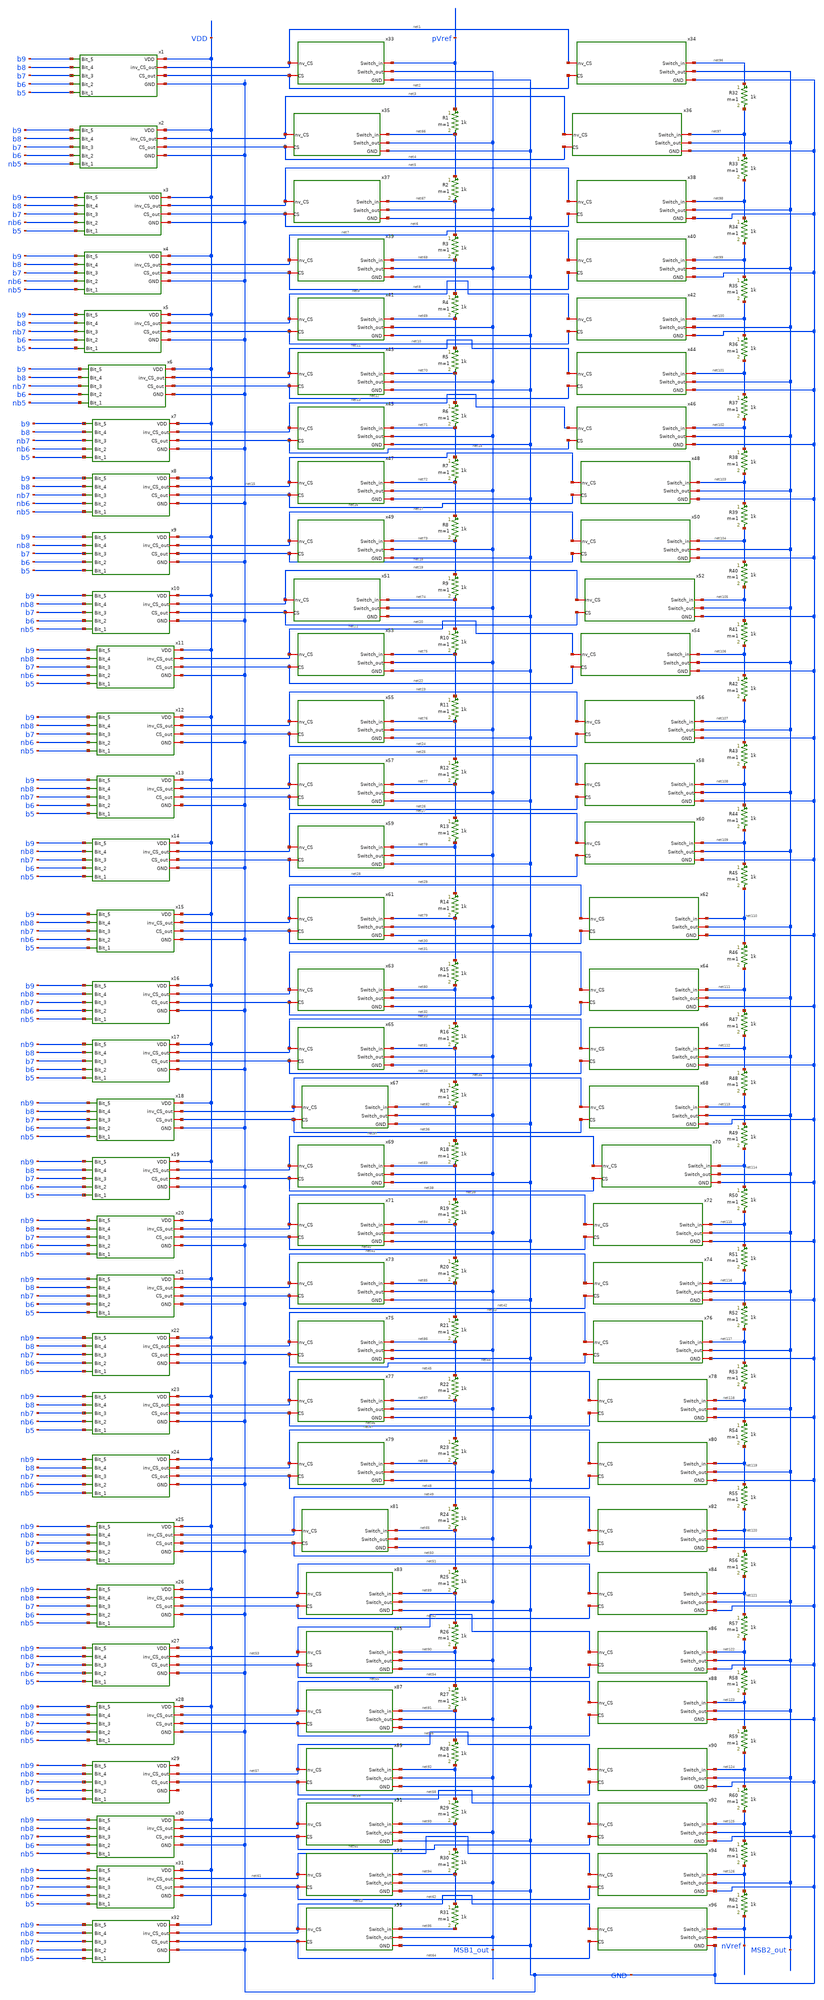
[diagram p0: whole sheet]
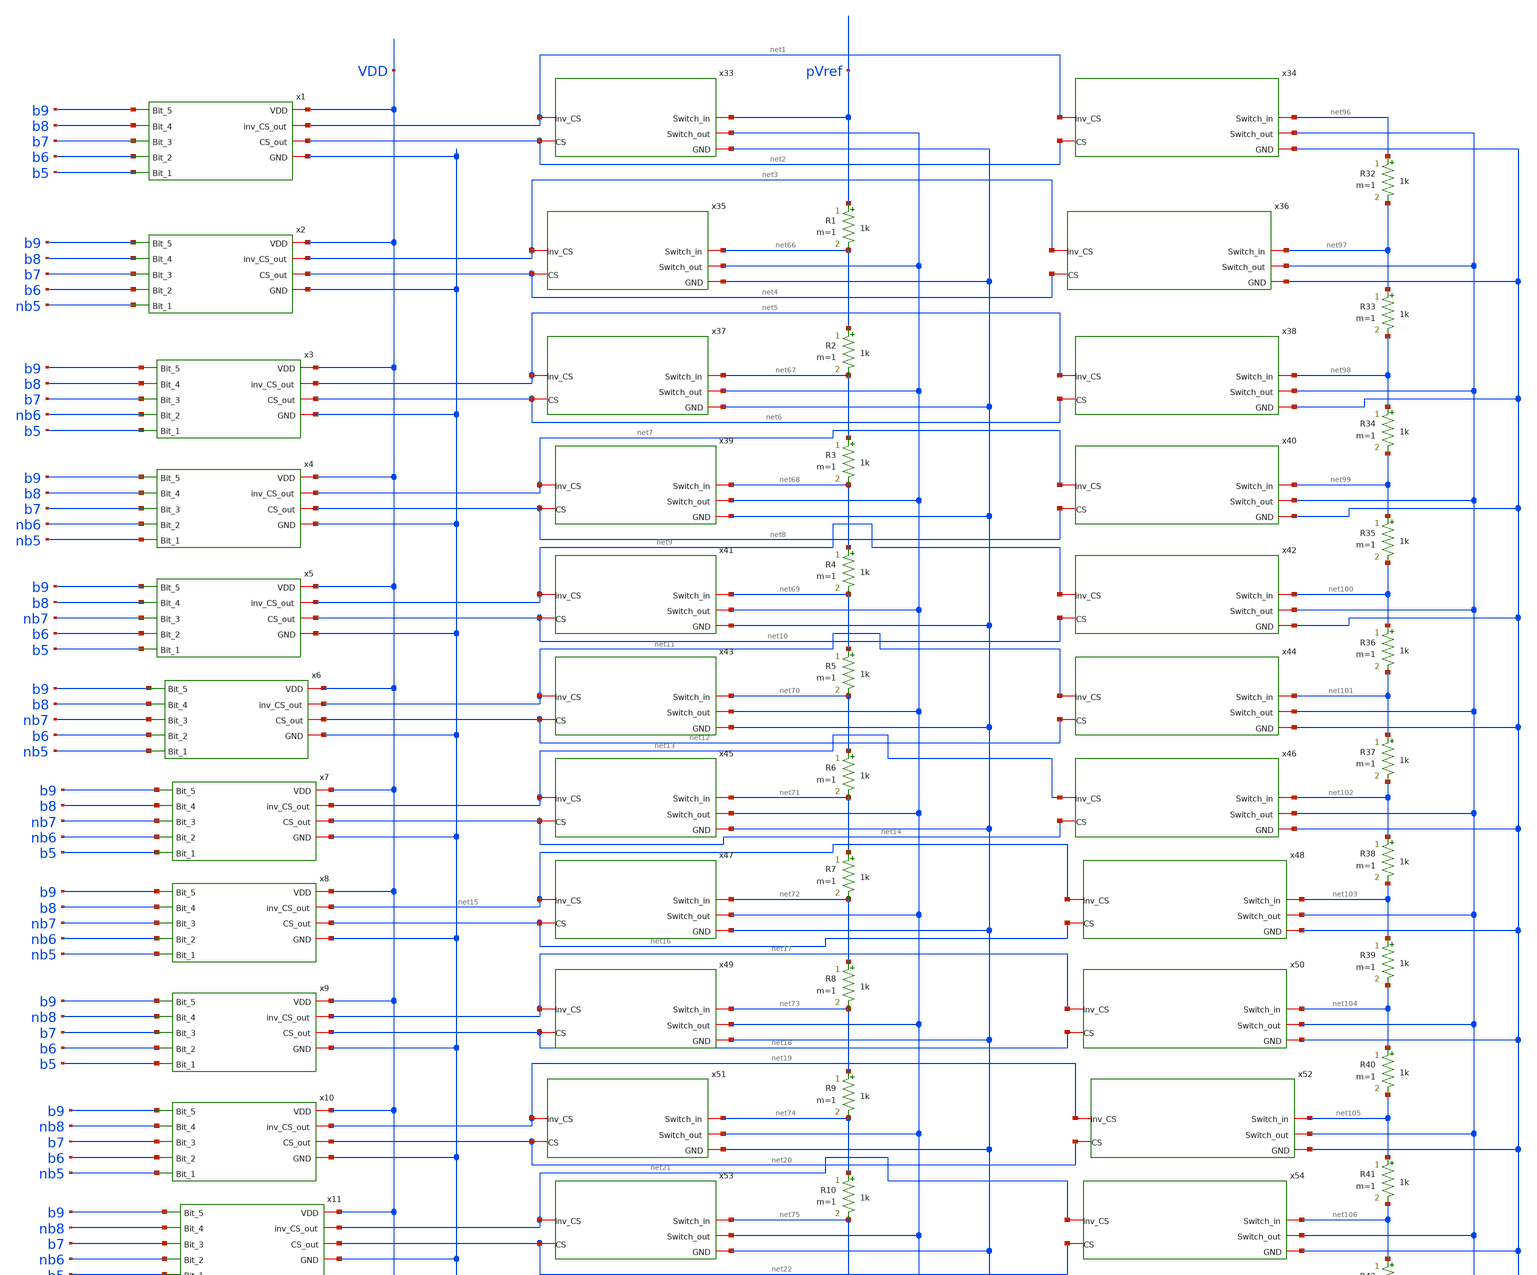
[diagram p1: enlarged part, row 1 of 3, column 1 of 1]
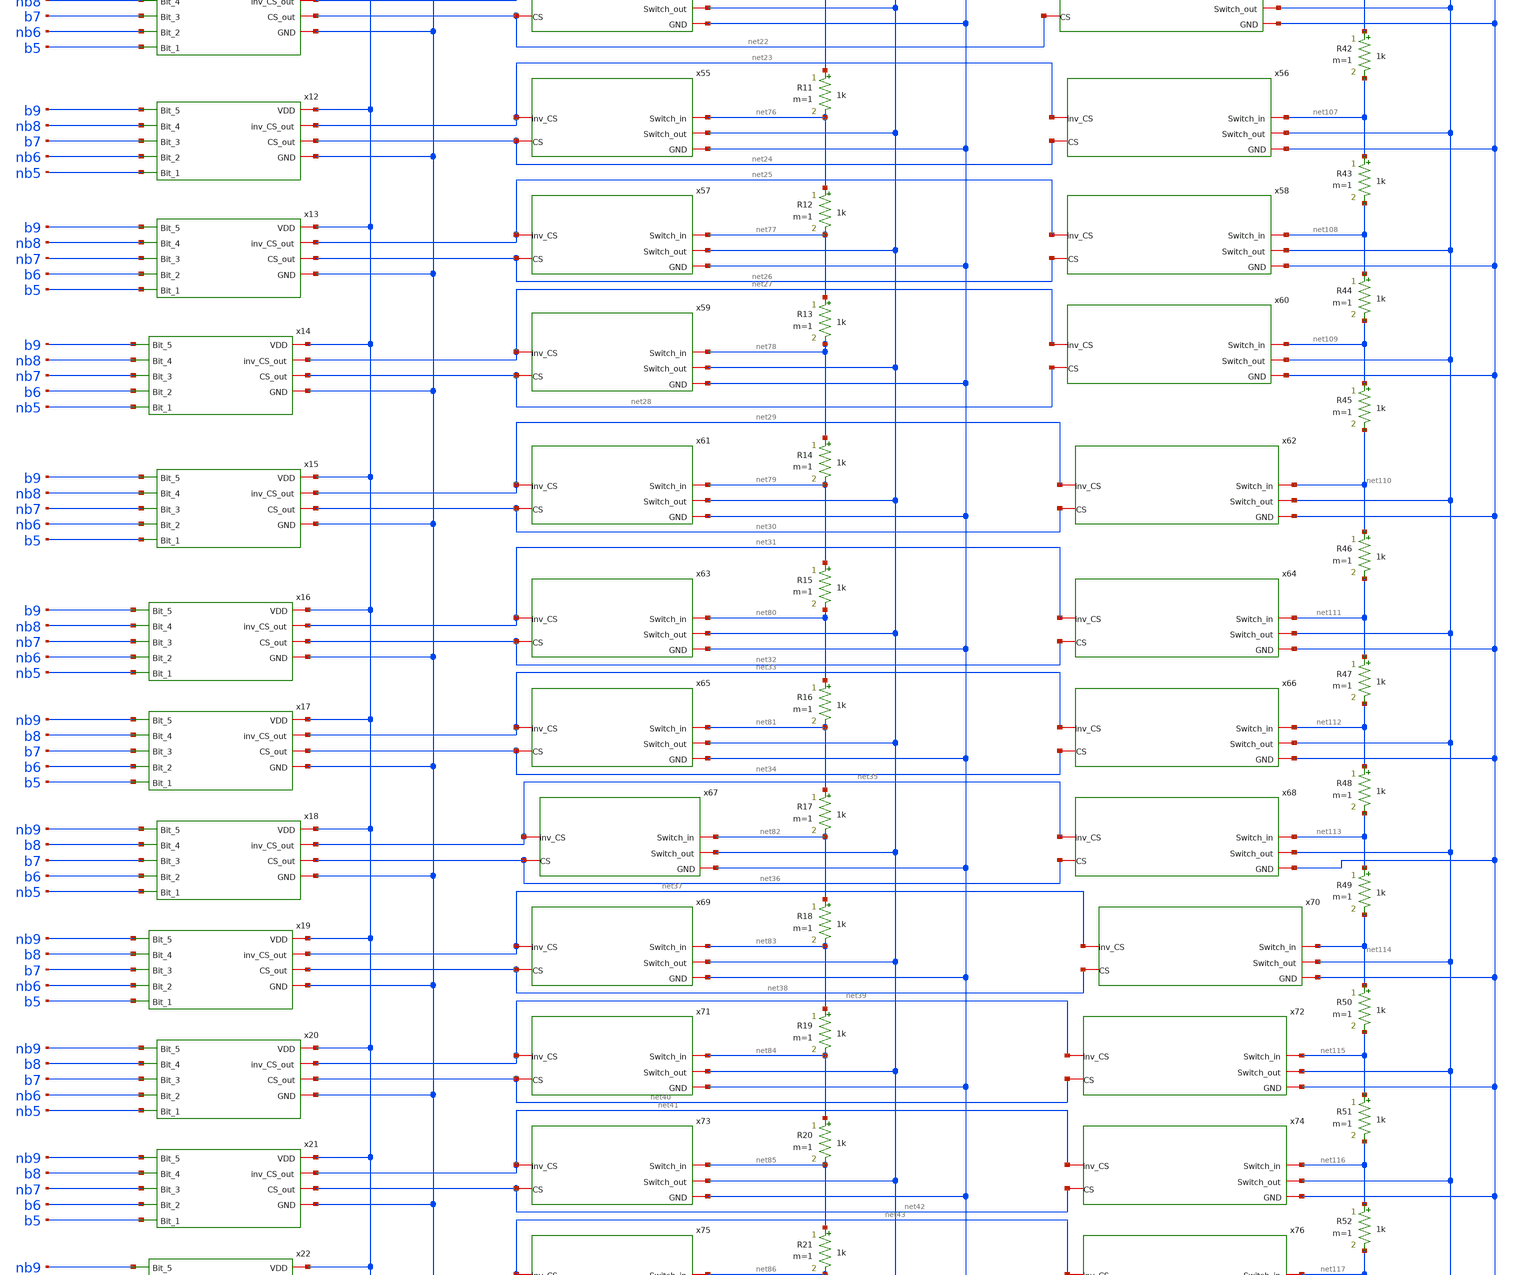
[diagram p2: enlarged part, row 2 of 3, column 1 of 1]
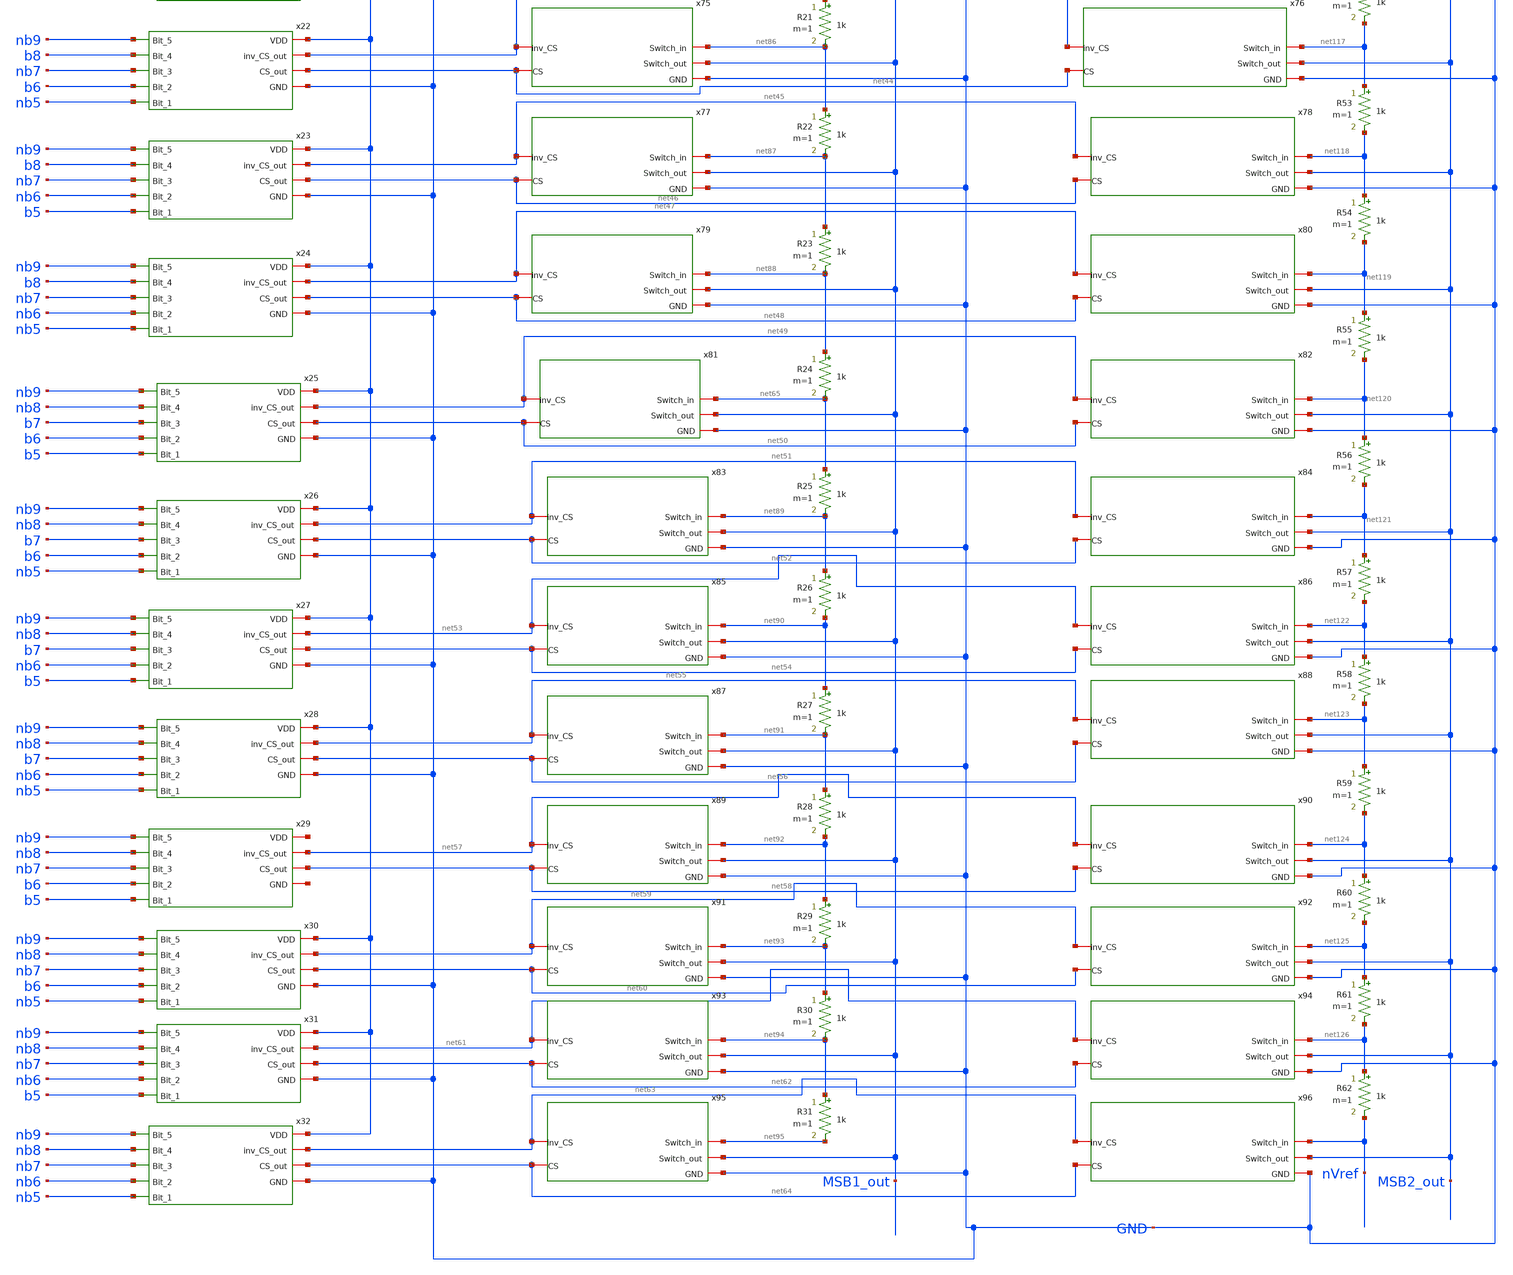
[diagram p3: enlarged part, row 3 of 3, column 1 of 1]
** sch_path: ProjectDesigns/10bitDAC/MSB.sch
**.subckt MSB
x1 VDD net1 b9 b8 net2 b7 b6 b5 GND 5bit_AND
x3 VDD net5 b9 b8 net6 b7 nb6 b5 GND 5bit_AND
x4 VDD net7 b9 b8 net8 b7 nb6 nb5 GND 5bit_AND
x5 VDD net9 b9 b8 net10 nb7 b6 b5 GND 5bit_AND
x6 VDD net11 b9 b8 net12 nb7 b6 nb5 GND 5bit_AND
x7 VDD net13 b9 b8 net14 nb7 nb6 b5 GND 5bit_AND
x8 VDD net15 b9 b8 net16 nb7 nb6 nb5 GND 5bit_AND
x9 VDD net17 b9 nb8 net18 b7 b6 b5 GND 5bit_AND
x2 VDD net3 b9 b8 net4 b7 b6 nb5 GND 5bit_AND
x10 VDD net19 b9 nb8 net20 b7 b6 nb5 GND 5bit_AND
x11 VDD net21 b9 nb8 net22 b7 nb6 b5 GND 5bit_AND
x12 VDD net23 b9 nb8 net24 b7 nb6 nb5 GND 5bit_AND
x13 VDD net25 b9 nb8 net26 nb7 b6 b5 GND 5bit_AND
x14 VDD net27 b9 nb8 net28 nb7 b6 nb5 GND 5bit_AND
x15 VDD net29 b9 nb8 net30 nb7 nb6 b5 GND 5bit_AND
x16 VDD net31 b9 nb8 net32 nb7 nb6 nb5 GND 5bit_AND
x17 VDD net33 nb9 b8 net34 b7 b6 b5 GND 5bit_AND
x18 VDD net35 nb9 b8 net36 b7 b6 nb5 GND 5bit_AND
x19 VDD net37 nb9 b8 net38 b7 nb6 b5 GND 5bit_AND
x20 VDD net39 nb9 b8 net40 b7 nb6 nb5 GND 5bit_AND
x21 VDD net41 nb9 b8 net42 nb7 b6 b5 GND 5bit_AND
x22 VDD net43 nb9 b8 net44 nb7 b6 nb5 GND 5bit_AND
x23 VDD net45 nb9 b8 net46 nb7 nb6 b5 GND 5bit_AND
x24 VDD net47 nb9 b8 net48 nb7 nb6 nb5 GND 5bit_AND
x25 VDD net49 nb9 nb8 net50 b7 b6 b5 GND 5bit_AND
x26 VDD net51 nb9 nb8 net52 b7 b6 nb5 GND 5bit_AND
x27 VDD net53 nb9 nb8 net54 b7 nb6 b5 GND 5bit_AND
x28 VDD net55 nb9 nb8 net56 b7 nb6 nb5 GND 5bit_AND
x29 net127 net57 nb9 nb8 net58 nb7 b6 b5 net128 5bit_AND
x30 VDD net59 nb9 nb8 net60 nb7 b6 nb5 GND 5bit_AND
x31 VDD net61 nb9 nb8 net62 nb7 nb6 b5 GND 5bit_AND
x32 VDD net63 nb9 nb8 net64 nb7 nb6 nb5 GND 5bit_AND
x33 net1 net2 pVref MSB1_out GND Switch
x34 net1 net2 net96 MSB2_out GND Switch
x35 net3 net4 net66 MSB1_out GND Switch
x36 net3 net4 net97 MSB2_out GND Switch
x37 net5 net6 net67 MSB1_out GND Switch
x38 net5 net6 net98 MSB2_out GND Switch
x39 net7 net8 net68 MSB1_out GND Switch
x40 net7 net8 net99 MSB2_out GND Switch
x41 net9 net10 net69 MSB1_out GND Switch
x42 net9 net10 net100 MSB2_out GND Switch
x43 net11 net12 net70 MSB1_out GND Switch
x44 net11 net12 net101 MSB2_out GND Switch
x45 net13 net14 net71 MSB1_out GND Switch
x46 net13 net14 net102 MSB2_out GND Switch
x47 net15 net16 net72 MSB1_out GND Switch
x48 net15 net16 net103 MSB2_out GND Switch
x49 net17 net18 net73 MSB1_out GND Switch
x50 net17 net18 net104 MSB2_out GND Switch
x51 net19 net20 net74 MSB1_out GND Switch
x52 net19 net20 net105 MSB2_out GND Switch
x53 net21 net22 net75 MSB1_out GND Switch
x54 net21 net22 net106 MSB2_out GND Switch
x55 net23 net24 net76 MSB1_out GND Switch
x56 net23 net24 net107 MSB2_out GND Switch
x57 net25 net26 net77 MSB1_out GND Switch
x58 net25 net26 net108 MSB2_out GND Switch
x59 net27 net28 net78 MSB1_out GND Switch
x60 net27 net28 net109 MSB2_out GND Switch
x61 net29 net30 net79 MSB1_out GND Switch
x62 net29 net30 net110 MSB2_out GND Switch
x63 net31 net32 net80 MSB1_out GND Switch
x64 net31 net32 net111 MSB2_out GND Switch
x65 net33 net34 net81 MSB1_out GND Switch
x66 net33 net34 net112 MSB2_out GND Switch
x67 net35 net36 net82 MSB1_out GND Switch
x68 net35 net36 net113 MSB2_out GND Switch
x69 net37 net38 net83 MSB1_out GND Switch
x70 net37 net38 net114 MSB2_out GND Switch
x71 net39 net40 net84 MSB1_out GND Switch
x72 net39 net40 net115 MSB2_out GND Switch
x73 net41 net42 net85 MSB1_out GND Switch
x74 net41 net42 net116 MSB2_out GND Switch
x75 net43 net44 net86 MSB1_out GND Switch
x76 net43 net44 net117 MSB2_out GND Switch
x77 net45 net46 net87 MSB1_out GND Switch
x78 net45 net46 net118 MSB2_out GND Switch
x79 net47 net48 net88 MSB1_out GND Switch
x80 net47 net48 net119 MSB2_out GND Switch
x81 net49 net50 net65 MSB1_out GND Switch
x82 net49 net50 net120 MSB2_out GND Switch
x83 net51 net52 net89 MSB1_out GND Switch
x84 net51 net52 net121 MSB2_out GND Switch
x85 net53 net54 net90 MSB1_out GND Switch
x86 net53 net54 net122 MSB2_out GND Switch
x87 net55 net56 net91 MSB1_out GND Switch
x88 net55 net56 net123 MSB2_out GND Switch
x89 net57 net58 net92 MSB1_out GND Switch
x90 net57 net58 net124 MSB2_out GND Switch
x91 net59 net60 net93 MSB1_out GND Switch
x92 net59 net60 net125 MSB2_out GND Switch
x93 net61 net62 net94 MSB1_out GND Switch
x94 net61 net62 net126 MSB2_out GND Switch
x95 net63 net64 net95 MSB1_out GND Switch
x96 net63 net64 nVref MSB2_out GND Switch
R1 pVref net66 1k m=1
R2 net66 net67 1k m=1
R3 net67 net68 1k m=1
R4 net68 net69 1k m=1
R5 net69 net70 1k m=1
R6 net70 net71 1k m=1
R7 net71 net72 1k m=1
R8 net72 net73 1k m=1
R9 net73 net74 1k m=1
R10 net74 net75 1k m=1
R11 net75 net76 1k m=1
R12 net76 net77 1k m=1
R13 net77 net78 1k m=1
R14 net78 net79 1k m=1
R15 net79 net80 1k m=1
R16 net80 net81 1k m=1
R17 net81 net82 1k m=1
R18 net82 net83 1k m=1
R19 net83 net84 1k m=1
R20 net84 net85 1k m=1
R21 net85 net86 1k m=1
R22 net86 net87 1k m=1
R23 net87 net88 1k m=1
R24 net88 net65 1k m=1
R25 net65 net89 1k m=1
R26 net89 net90 1k m=1
R27 net90 net91 1k m=1
R28 net91 net92 1k m=1
R29 net92 net93 1k m=1
R30 net93 net94 1k m=1
R31 net94 net95 1k m=1
R32 net96 net97 1k m=1
R33 net97 net98 1k m=1
R34 net98 net99 1k m=1
R35 net99 net100 1k m=1
R36 net100 net101 1k m=1
R37 net101 net102 1k m=1
R38 net102 net103 1k m=1
R39 net103 net104 1k m=1
R40 net104 net105 1k m=1
R41 net105 net106 1k m=1
R42 net106 net107 1k m=1
R43 net107 net108 1k m=1
R44 net108 net109 1k m=1
R45 net109 net110 1k m=1
R46 net110 net111 1k m=1
R47 net111 net112 1k m=1
R48 net112 net113 1k m=1
R49 net113 net114 1k m=1
R50 net114 net115 1k m=1
R51 net115 net116 1k m=1
R52 net116 net117 1k m=1
R53 net117 net118 1k m=1
R54 net118 net119 1k m=1
R55 net119 net120 1k m=1
R56 net120 net121 1k m=1
R57 net121 net122 1k m=1
R58 net122 net123 1k m=1
R59 net123 net124 1k m=1
R60 net124 net125 1k m=1
R61 net125 net126 1k m=1
R62 net126 nVref 1k m=1
**.ends

* expanding   symbol:  /home/shalini1234/Project/5bit_AND.sym # of pins=9
** sym_path: ProjectDesigns/5BitAND/5bit_AND.sym
** sch_path: ProjectDesigns/5BitAND/5bit_AND.sch
.subckt 5bit_AND VDD inv_CS_out Bit_5 Bit_4 CS_out Bit_3 Bit_2 Bit_1 GND
*.ipin Bit_1
*.ipin Bit_3
*.ipin Bit_2
*.ipin Bit_4
*.ipin Bit_5
*.iopin inv_CS_out
*.iopin CS_out
*.iopin VDD
*.iopin GND
XM1 inv_CS_out Bit_5 net1 net1 sky130_fd_pr__nfet_01v8 L=0.15 W=1 nf=1 ad='int((nf+1)/2) * W/nf * 0.29'
+ as='int((nf+2)/2) * W/nf * 0.29' pd='2*int((nf+1)/2) * (W/nf + 0.29)' ps='2*int((nf+2)/2) * (W/nf + 0.29)'
+ nrd='0.29 / W' nrs='0.29 / W' sa=0 sb=0 sd=0 mult=1 m=1
XM2 net1 Bit_4 net2 net2 sky130_fd_pr__nfet_01v8 L=0.15 W=1 nf=1 ad='int((nf+1)/2) * W/nf * 0.29' as='int((nf+2)/2) * W/nf * 0.29'
+ pd='2*int((nf+1)/2) * (W/nf + 0.29)' ps='2*int((nf+2)/2) * (W/nf + 0.29)' nrd='0.29 / W' nrs='0.29 / W'
+ sa=0 sb=0 sd=0 mult=1 m=1
XM3 net2 Bit_3 net3 net3 sky130_fd_pr__nfet_01v8 L=0.15 W=1 nf=1 ad='int((nf+1)/2) * W/nf * 0.29' as='int((nf+2)/2) * W/nf * 0.29'
+ pd='2*int((nf+1)/2) * (W/nf + 0.29)' ps='2*int((nf+2)/2) * (W/nf + 0.29)' nrd='0.29 / W' nrs='0.29 / W'
+ sa=0 sb=0 sd=0 mult=1 m=1
XM4 net3 Bit_2 net4 net4 sky130_fd_pr__nfet_01v8 L=0.15 W=1 nf=1 ad='int((nf+1)/2) * W/nf * 0.29' as='int((nf+2)/2) * W/nf * 0.29'
+ pd='2*int((nf+1)/2) * (W/nf + 0.29)' ps='2*int((nf+2)/2) * (W/nf + 0.29)' nrd='0.29 / W' nrs='0.29 / W'
+ sa=0 sb=0 sd=0 mult=1 m=1
XM5 net4 Bit_1 GND GND sky130_fd_pr__nfet_01v8 L=0.15 W=1 nf=1 ad='int((nf+1)/2) * W/nf * 0.29' as='int((nf+2)/2) * W/nf * 0.29'
+ pd='2*int((nf+1)/2) * (W/nf + 0.29)' ps='2*int((nf+2)/2) * (W/nf + 0.29)' nrd='0.29 / W' nrs='0.29 / W'
+ sa=0 sb=0 sd=0 mult=1 m=1
XM6 inv_CS_out Bit_3 VDD VDD sky130_fd_pr__pfet_01v8 L=0.15 W=1 nf=1 ad='int((nf+1)/2) * W/nf * 0.29'
+ as='int((nf+2)/2) * W/nf * 0.29' pd='2*int((nf+1)/2) * (W/nf + 0.29)' ps='2*int((nf+2)/2) * (W/nf + 0.29)'
+ nrd='0.29 / W' nrs='0.29 / W' sa=0 sb=0 sd=0 mult=1 m=1
XM7 inv_CS_out Bit_2 VDD VDD sky130_fd_pr__pfet_01v8 L=0.15 W=1 nf=1 ad='int((nf+1)/2) * W/nf * 0.29'
+ as='int((nf+2)/2) * W/nf * 0.29' pd='2*int((nf+1)/2) * (W/nf + 0.29)' ps='2*int((nf+2)/2) * (W/nf + 0.29)'
+ nrd='0.29 / W' nrs='0.29 / W' sa=0 sb=0 sd=0 mult=1 m=1
XM8 inv_CS_out Bit_1 VDD VDD sky130_fd_pr__pfet_01v8 L=0.15 W=1 nf=1 ad='int((nf+1)/2) * W/nf * 0.29'
+ as='int((nf+2)/2) * W/nf * 0.29' pd='2*int((nf+1)/2) * (W/nf + 0.29)' ps='2*int((nf+2)/2) * (W/nf + 0.29)'
+ nrd='0.29 / W' nrs='0.29 / W' sa=0 sb=0 sd=0 mult=1 m=1
XM9 inv_CS_out Bit_4 VDD VDD sky130_fd_pr__pfet_01v8 L=0.15 W=1 nf=1 ad='int((nf+1)/2) * W/nf * 0.29'
+ as='int((nf+2)/2) * W/nf * 0.29' pd='2*int((nf+1)/2) * (W/nf + 0.29)' ps='2*int((nf+2)/2) * (W/nf + 0.29)'
+ nrd='0.29 / W' nrs='0.29 / W' sa=0 sb=0 sd=0 mult=1 m=1
XM10 inv_CS_out Bit_5 VDD VDD sky130_fd_pr__pfet_01v8 L=0.15 W=1 nf=1 ad='int((nf+1)/2) * W/nf * 0.29'
+ as='int((nf+2)/2) * W/nf * 0.29' pd='2*int((nf+1)/2) * (W/nf + 0.29)' ps='2*int((nf+2)/2) * (W/nf + 0.29)'
+ nrd='0.29 / W' nrs='0.29 / W' sa=0 sb=0 sd=0 mult=1 m=1
XM11 CS_out inv_CS_out GND GND sky130_fd_pr__nfet_01v8 L=0.15 W=1 nf=1 ad='int((nf+1)/2) * W/nf * 0.29'
+ as='int((nf+2)/2) * W/nf * 0.29' pd='2*int((nf+1)/2) * (W/nf + 0.29)' ps='2*int((nf+2)/2) * (W/nf + 0.29)'
+ nrd='0.29 / W' nrs='0.29 / W' sa=0 sb=0 sd=0 mult=1 m=1
XM12 CS_out inv_CS_out VDD VDD sky130_fd_pr__pfet_01v8 L=0.15 W=1 nf=1 ad='int((nf+1)/2) * W/nf * 0.29'
+ as='int((nf+2)/2) * W/nf * 0.29' pd='2*int((nf+1)/2) * (W/nf + 0.29)' ps='2*int((nf+2)/2) * (W/nf + 0.29)'
+ nrd='0.29 / W' nrs='0.29 / W' sa=0 sb=0 sd=0 mult=1 m=1
.ends


* expanding   symbol:  /home/shalini1234/Project/Switch.sym # of pins=5
** sym_path: ProjectDesigns/Switch/Switch.sym
** sch_path: ProjectDesigns/Switch/Switch.sch
.subckt Switch inv_CS CS Switch_in Switch_out GND
*.iopin Switch_in
*.iopin Switch_out
*.iopin CS
*.iopin inv_CS
*.iopin GND
XM1 Switch_in CS Switch_out Switch_out sky130_fd_pr__nfet_01v8 L=0.15 W=1 nf=1 ad='int((nf+1)/2) * W/nf * 0.29'
+ as='int((nf+2)/2) * W/nf * 0.29' pd='2*int((nf+1)/2) * (W/nf + 0.29)' ps='2*int((nf+2)/2) * (W/nf + 0.29)'
+ nrd='0.29 / W' nrs='0.29 / W' sa=0 sb=0 sd=0 mult=1 m=1
XM2 Switch_out inv_CS Switch_in Switch_in sky130_fd_pr__pfet_01v8 L=0.15 W=1 nf=1 ad='int((nf+1)/2) * W/nf * 0.29'
+ as='int((nf+2)/2) * W/nf * 0.29' pd='2*int((nf+1)/2) * (W/nf + 0.29)' ps='2*int((nf+2)/2) * (W/nf + 0.29)'
+ nrd='0.29 / W' nrs='0.29 / W' sa=0 sb=0 sd=0 mult=1 m=1
XM5 Switch_out inv_CS GND GND sky130_fd_pr__nfet_01v8 L=0.15 W=1 nf=1 ad='int((nf+1)/2) * W/nf * 0.29'
+ as='int((nf+2)/2) * W/nf * 0.29' pd='2*int((nf+1)/2) * (W/nf + 0.29)' ps='2*int((nf+2)/2) * (W/nf + 0.29)'
+ nrd='0.29 / W' nrs='0.29 / W' sa=0 sb=0 sd=0 mult=1 m=1
.ends

.end
